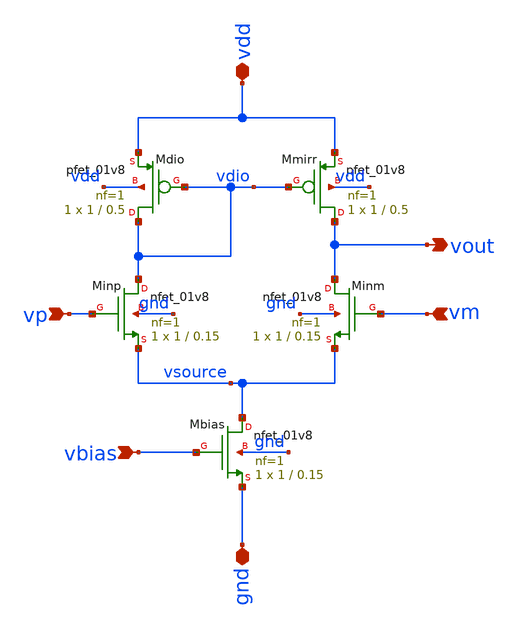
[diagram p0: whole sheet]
** sch_path: analog/klayout/production/final_merge_20260923/testbenches/cace/analog/xschem/amp_n.sch
**.subckt amp_n gnd vdd vp vm vout vbias
*.iopin gnd
*.iopin vdd
*.ipin vp
*.ipin vm
*.opin vout
*.ipin vbias
XMmirr vout vdio vdd vdd sky130_fd_pr__pfet_01v8 L=0.5 W=1 nf=1 ad='int((1 + 1)/2) * 1 / 1 * 0.29' as='int((1 + 2)/2) * 1 / 1 * 0.29'
+ pd='2*int((1 + 1)/2) * (1 / 1 + 0.29)' ps='2*int((1 + 2)/2) * (1 / 1 + 0.29)' nrd='0.29 / 1 ' nrs='0.29 / 1 '
+ sa=0 sb=0 sd=0 mult=1 m=1
XMdio vdio vdio vdd vdd sky130_fd_pr__pfet_01v8 L=0.5 W=1 nf=1 ad='int((1 + 1)/2) * 1 / 1 * 0.29' as='int((1 + 2)/2) * 1 / 1 * 0.29'
+ pd='2*int((1 + 1)/2) * (1 / 1 + 0.29)' ps='2*int((1 + 2)/2) * (1 / 1 + 0.29)' nrd='0.29 / 1 ' nrs='0.29 / 1 '
+ sa=0 sb=0 sd=0 mult=1 m=1
XMinp vdio vp vsource gnd sky130_fd_pr__nfet_01v8 L=0.15 W=1 nf=1 ad='int((1 + 1)/2) * 1 / 1 * 0.29'
+ as='int((1 + 2)/2) * 1 / 1 * 0.29' pd='2*int((1 + 1)/2) * (1 / 1 + 0.29)' ps='2*int((1 + 2)/2) * (1 / 1 + 0.29)'
+ nrd='0.29 / 1 ' nrs='0.29 / 1 ' sa=0 sb=0 sd=0 mult=1 m=1
XMinm vout vm vsource gnd sky130_fd_pr__nfet_01v8 L=0.15 W=1 nf=1 ad='int((1 + 1)/2) * 1 / 1 * 0.29'
+ as='int((1 + 2)/2) * 1 / 1 * 0.29' pd='2*int((1 + 1)/2) * (1 / 1 + 0.29)' ps='2*int((1 + 2)/2) * (1 / 1 + 0.29)'
+ nrd='0.29 / 1 ' nrs='0.29 / 1 ' sa=0 sb=0 sd=0 mult=1 m=1
XMbias vsource vbias gnd gnd sky130_fd_pr__nfet_01v8 L=0.15 W=1 nf=1 ad='int((1 + 1)/2) * 1 / 1 * 0.29'
+ as='int((1 + 2)/2) * 1 / 1 * 0.29' pd='2*int((1 + 1)/2) * (1 / 1 + 0.29)' ps='2*int((1 + 2)/2) * (1 / 1 + 0.29)'
+ nrd='0.29 / 1 ' nrs='0.29 / 1 ' sa=0 sb=0 sd=0 mult=1 m=1
**.ends
.end
